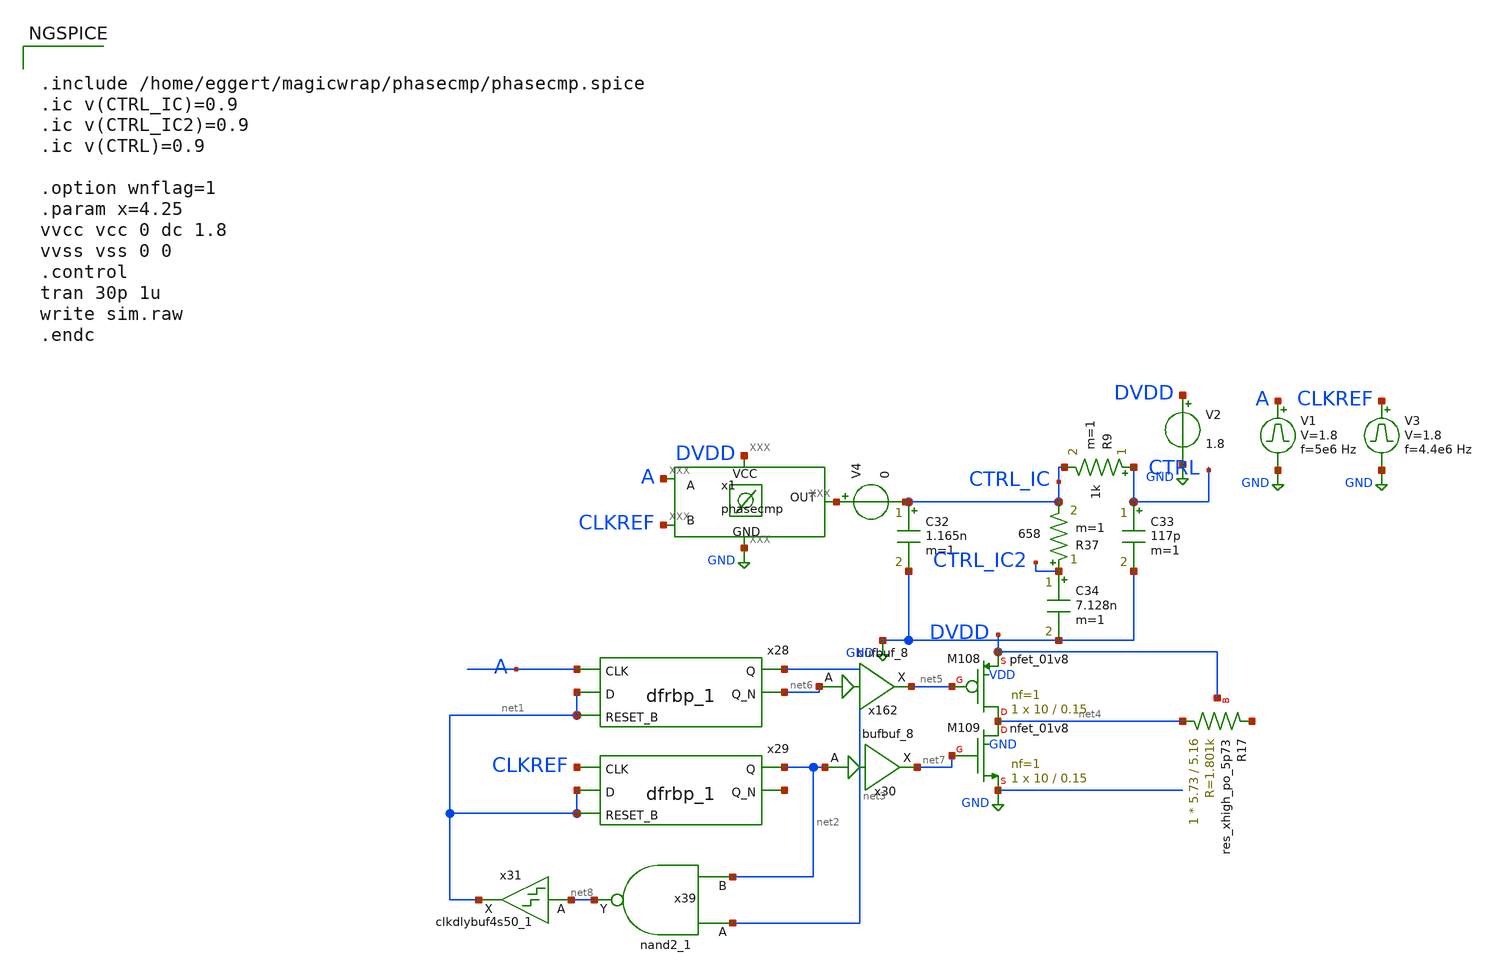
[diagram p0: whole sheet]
** sch_path: xschem/xschemwrap/phasecmp_test.sch
**.subckt phasecmp_test
x28 A net1 net1 VSS VSS VCC VCC net3 net6 sky130_fd_sc_hd__dfrbp_1
x29 CLKREF net1 net1 VSS VSS VCC VCC net2 net9 sky130_fd_sc_hd__dfrbp_1
x39 net3 net2 VSS VSS VCC VCC net8 sky130_fd_sc_hd__nand2_1
XM108 net4 net5 DVDD VDD sky130_fd_pr__pfet_01v8 L=0.15 W=10 nf=1 ad='int((1 + 1)/2) * 10 / 1 * 0.29'
+ as='int((1 + 2)/2) * 10 / 1 * 0.29' pd='2*int((1 + 1)/2) * (10 / 1 + 0.29)' ps='2*int((1 + 2)/2) * (10 / 1 + 0.29)'
+ nrd='0.29 / 10 ' nrs='0.29 / 10 ' sa=0 sb=0 sd=0 mult=1 m=1
XM109 net4 net7 GND GND sky130_fd_pr__nfet_01v8 L=0.15 W=10 nf=1 ad='int((nf+1)/2) * W/nf * 0.29' as='int((nf+2)/2) * W/nf * 0.29'
+ pd='2*int((nf+1)/2) * (W/nf + 0.29)' ps='2*int((nf+2)/2) * (W/nf + 0.29)' nrd='0.29 / W' nrs='0.29 / W'
+ sa=0 sb=0 sd=0 mult=1 m=1
x162 net6 VSS VSS VCC VCC net5 sky130_fd_sc_hd__bufbuf_8
x30 net2 VSS VSS VCC VCC net7 sky130_fd_sc_hd__bufbuf_8
x31 net8 VSS VSS VCC VCC net1 sky130_fd_sc_hd__clkdlybuf4s50_1
XR17 net4 net10 DVDD sky130_fd_pr__res_xhigh_po_5p73 L=5.16 mult=1 m=1
x1 GND phasecmp
V2 DVDD GND 1.8
V1 A GND pulse 0 1.8 '0.495/ 5e6 ' '0.01/5e6 ' '0.01/5e6 ' '0.49/5e6 ' '1/5e6 '
V3 CLKREF GND pulse 0 1.8 '0.495/ 4.4e6 ' '0.01/4.4e6 ' '0.01/4.4e6 ' '0.49/4.4e6 ' '1/4.4e6 '
C32 CTRL_IC GND 1.165n m=1
C33 CTRL GND 117p m=1
R9 CTRL CTRL_IC 1k m=1
R37 CTRL_IC2 CTRL_IC 658 m=1
C34 CTRL_IC2 GND 7.128n m=1
V4 GND CTRL_IC 0
**** begin user architecture code

** opencircuitdesign pdks install
.include /home/eggert/test.xspice
.lib $::SKYWATER_MODELS/sky130.lib.spice tt



.include /home/eggert/magicwrap/phasecmp/phasecmp.spice
.ic v(CTRL_IC)=0.9
.ic v(CTRL_IC2)=0.9
.ic v(CTRL)=0.9

.option wnflag=1
.param x=4.25
vvcc vcc 0 dc 1.8
vvss vss 0 0
.control
tran 30p 1u
write sim.raw
.endc


**** end user architecture code
**.ends
.GLOBAL GND
.end
